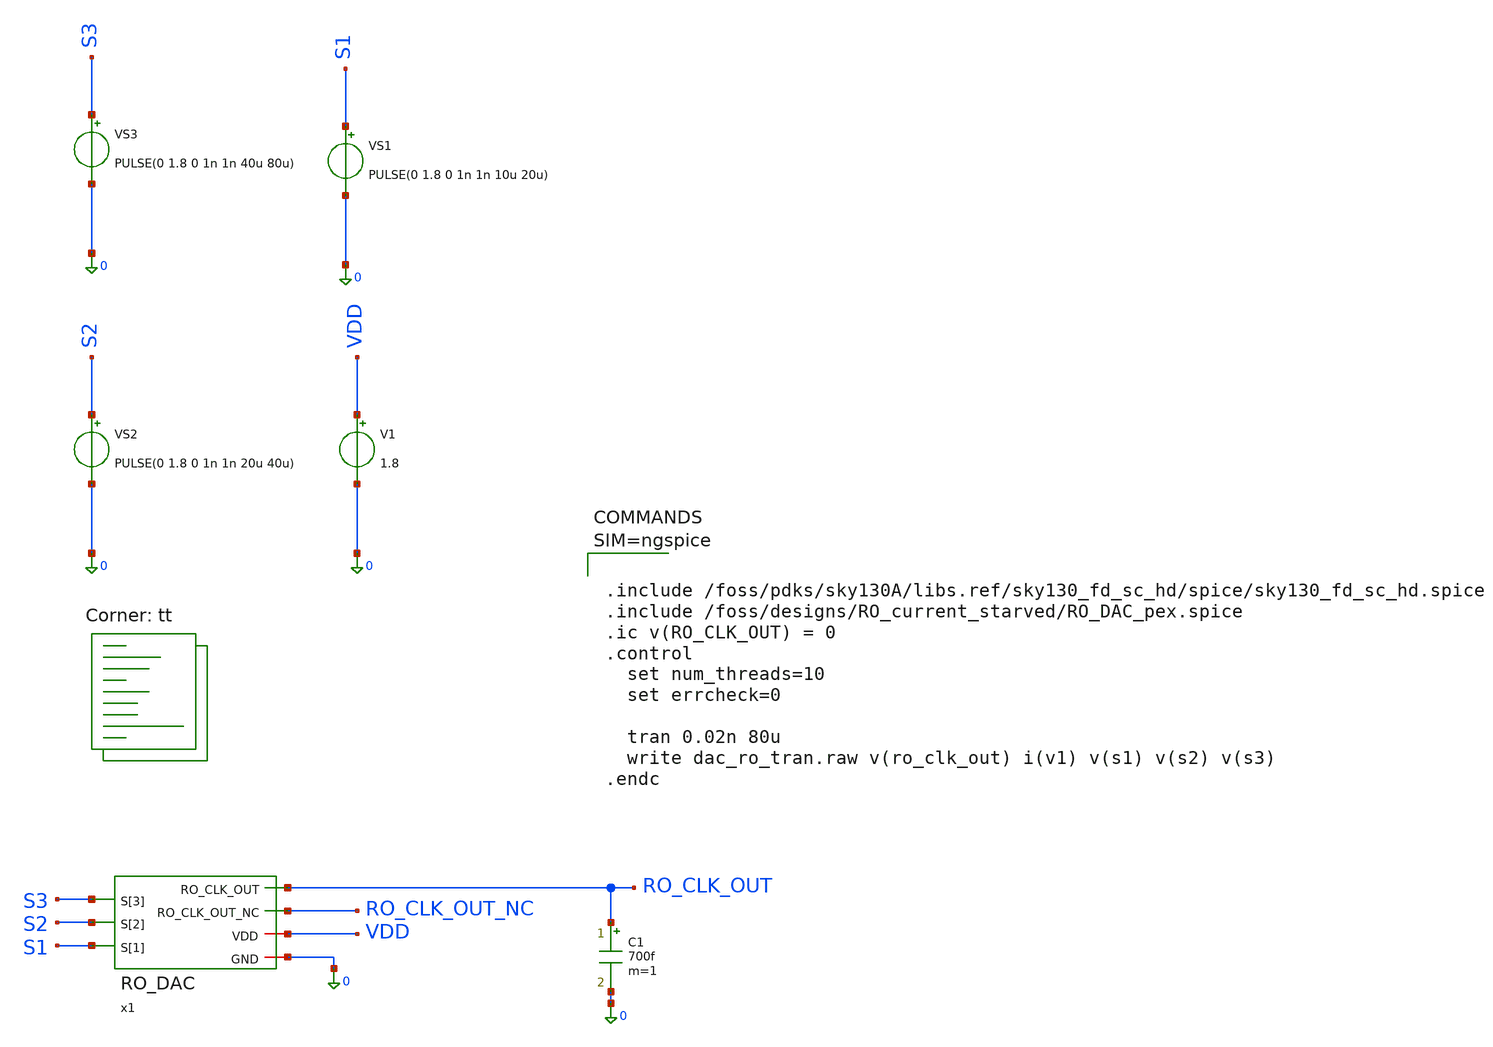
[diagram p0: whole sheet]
** sch_path: src/analog_source_files/RO_DAC_tb.sch
**.subckt RO_DAC_tb
x1 RO_CLK_OUT S3 RO_CLK_OUT_NC S2 S1 VDD 0 RO_DAC
V1 VDD 0 1.8
VS1 S1 0 PULSE(0 1.8 0 1n 1n 10u 20u)
VS2 S2 0 PULSE(0 1.8 0 1n 1n 20u 40u)
VS3 S3 0 PULSE(0 1.8 0 1n 1n 40u 80u)
C1 RO_CLK_OUT 0 700f m=1
**** begin user architecture code
.lib $::SKYWATER_MODELS/sky130.lib.spice tt



.include /foss/pdks/sky130A/libs.ref/sky130_fd_sc_hd/spice/sky130_fd_sc_hd.spice
.include /foss/designs/RO_current_starved/RO_DAC_pex.spice
.ic v(RO_CLK_OUT) = 0
.control
  set num_threads=10
  set errcheck=0

  tran 0.02n 80u
  write dac_ro_tran.raw v(ro_clk_out) i(v1) v(s1) v(s2) v(s3)
.endc



**** end user architecture code
**.ends
.end
